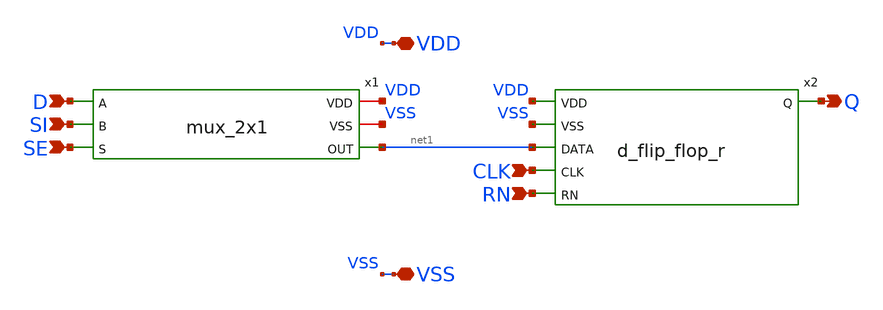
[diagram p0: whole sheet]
** sch_path: designs/cells/sdffrnq/sch/sdffrnq.sch
**.subckt sdffrnq D SI SE VDD VSS Q RN CLK
*.ipin D
*.ipin SI
*.ipin SE
*.iopin VDD
*.iopin VSS
*.opin Q
*.ipin RN
*.ipin CLK
x1 D SI VDD VSS SE net1 mux_2x1
x2 VDD VSS Q net1 CLK RN d_flip_flop_r
**.ends

* expanding   symbol:  cells/sdffrq/sch/mux_2x1.sym # of pins=6
** sym_path: designs/cells/sdffrq/sch/mux_2x1.sym
** sch_path: designs/cells/sdffrq/sch/mux_2x1.sch
.subckt mux_2x1 A B VDD VSS S OUT
*.iopin VDD
*.opin OUT
*.ipin A
*.ipin B
*.ipin S
*.iopin VSS
x1 VDD S A TG_OUT S_INV VSS mux_tg
x2 VDD S_INV B TG_OUT S VSS mux_tg
x3 VDD S S_INV VSS inv
x4 VDD TG_OUT net1 VSS inv
x5 VDD net1 OUT VSS inv
.ends


* expanding   symbol:  cells/sdffrq/sch/d_flip_flop_r.sym # of pins=6
** sym_path: designs/cells/gf180mcu_voidwalkers_sc_sdffrnq_4/sch/d_flip_flop_r.sym
** sch_path: designs/cells/gf180mcu_voidwalkers_sc_sdffrnq_4/sch/d_flip_flop_r.sch
.subckt d_flip_flop_r VDD VSS Q DATA CLK RN
*.ipin DATA
*.ipin VDD
*.ipin VSS
*.opin Q
*.ipin CLK
*.ipin RN
XM1 net1 DATA VDD VDD pfet_03v3 L=0.3u W=1.7u nf=1 ad='int((nf+1)/2) * W/nf * 0.18u' as='int((nf+2)/2) * W/nf * 0.18u'
+ pd='2*int((nf+1)/2) * (W/nf + 0.18u)' ps='2*int((nf+2)/2) * (W/nf + 0.18u)' nrd='0.18u / W' nrs='0.18u / W'
+ sa=0 sb=0 sd=0 m=1
XM2 PROBE[0] CLK_INV net2 VSS nfet_03v3 L=0.3u W=0.85u nf=1 ad='int((nf+1)/2) * W/nf * 0.18u' as='int((nf+2)/2) * W/nf * 0.18u'
+ pd='2*int((nf+1)/2) * (W/nf + 0.18u)' ps='2*int((nf+2)/2) * (W/nf + 0.18u)' nrd='0.18u / W' nrs='0.18u / W'
+ sa=0 sb=0 sd=0 m=1
XM3 PROBE[0] CLK net1 VDD pfet_03v3 L=0.3u W=1.7u nf=1 ad='int((nf+1)/2) * W/nf * 0.18u' as='int((nf+2)/2) * W/nf * 0.18u'
+ pd='2*int((nf+1)/2) * (W/nf + 0.18u)' ps='2*int((nf+2)/2) * (W/nf + 0.18u)' nrd='0.18u / W' nrs='0.18u / W'
+ sa=0 sb=0 sd=0 m=1
XM4 net2 DATA VSS VSS nfet_03v3 L=0.3u W=0.85u nf=1 ad='int((nf+1)/2) * W/nf * 0.18u' as='int((nf+2)/2) * W/nf * 0.18u'
+ pd='2*int((nf+1)/2) * (W/nf + 0.18u)' ps='2*int((nf+2)/2) * (W/nf + 0.18u)' nrd='0.18u / W' nrs='0.18u / W'
+ sa=0 sb=0 sd=0 m=1
XM5 CLK_INV_2 CLK VDD VDD pfet_03v3 L=0.3u W=1.7u nf=1 ad='int((nf+1)/2) * W/nf * 0.18u' as='int((nf+2)/2) * W/nf * 0.18u'
+ pd='2*int((nf+1)/2) * (W/nf + 0.18u)' ps='2*int((nf+2)/2) * (W/nf + 0.18u)' nrd='0.18u / W' nrs='0.18u / W'
+ sa=0 sb=0 sd=0 m=1
XM8 CLK_INV_2 CLK VSS VSS nfet_03v3 L=0.3u W=0.85u nf=1 ad='int((nf+1)/2) * W/nf * 0.18u' as='int((nf+2)/2) * W/nf * 0.18u'
+ pd='2*int((nf+1)/2) * (W/nf + 0.18u)' ps='2*int((nf+2)/2) * (W/nf + 0.18u)' nrd='0.18u / W' nrs='0.18u / W'
+ sa=0 sb=0 sd=0 m=1
XM13 net3 PROBE[1] VDD VDD pfet_03v3 L=0.3u W=1.7u nf=1 ad='int((nf+1)/2) * W/nf * 0.18u' as='int((nf+2)/2) * W/nf * 0.18u'
+ pd='2*int((nf+1)/2) * (W/nf + 0.18u)' ps='2*int((nf+2)/2) * (W/nf + 0.18u)' nrd='0.18u / W' nrs='0.18u / W'
+ sa=0 sb=0 sd=0 m=1
XM14 PROBE[0] CLK net4 VSS nfet_03v3 L=0.3u W=0.85u nf=1 ad='int((nf+1)/2) * W/nf * 0.18u' as='int((nf+2)/2) * W/nf * 0.18u'
+ pd='2*int((nf+1)/2) * (W/nf + 0.18u)' ps='2*int((nf+2)/2) * (W/nf + 0.18u)' nrd='0.18u / W' nrs='0.18u / W'
+ sa=0 sb=0 sd=0 m=1
XM15 PROBE[0] CLK_INV net3 VDD pfet_03v3 L=0.3u W=1.7u nf=1 ad='int((nf+1)/2) * W/nf * 0.18u' as='int((nf+2)/2) * W/nf * 0.18u'
+ pd='2*int((nf+1)/2) * (W/nf + 0.18u)' ps='2*int((nf+2)/2) * (W/nf + 0.18u)' nrd='0.18u / W' nrs='0.18u / W'
+ sa=0 sb=0 sd=0 m=1
XM16 net4 PROBE[1] VSS VSS nfet_03v3 L=0.3u W=0.85u nf=1 ad='int((nf+1)/2) * W/nf * 0.18u' as='int((nf+2)/2) * W/nf * 0.18u'
+ pd='2*int((nf+1)/2) * (W/nf + 0.18u)' ps='2*int((nf+2)/2) * (W/nf + 0.18u)' nrd='0.18u / W' nrs='0.18u / W'
+ sa=0 sb=0 sd=0 m=1
XM9 net5 PROBE[1] VDD VDD pfet_03v3 L=0.3u W=1.7u nf=1 ad='int((nf+1)/2) * W/nf * 0.18u' as='int((nf+2)/2) * W/nf * 0.18u'
+ pd='2*int((nf+1)/2) * (W/nf + 0.18u)' ps='2*int((nf+2)/2) * (W/nf + 0.18u)' nrd='0.18u / W' nrs='0.18u / W'
+ sa=0 sb=0 sd=0 m=1
XM10 PROBE[2] CLK net6 VSS nfet_03v3 L=0.3u W=0.85u nf=1 ad='int((nf+1)/2) * W/nf * 0.18u' as='int((nf+2)/2) * W/nf * 0.18u'
+ pd='2*int((nf+1)/2) * (W/nf + 0.18u)' ps='2*int((nf+2)/2) * (W/nf + 0.18u)' nrd='0.18u / W' nrs='0.18u / W'
+ sa=0 sb=0 sd=0 m=1
XM11 PROBE[2] CLK_INV_2 net5 VDD pfet_03v3 L=0.3u W=1.7u nf=1 ad='int((nf+1)/2) * W/nf * 0.18u' as='int((nf+2)/2) * W/nf * 0.18u'
+ pd='2*int((nf+1)/2) * (W/nf + 0.18u)' ps='2*int((nf+2)/2) * (W/nf + 0.18u)' nrd='0.18u / W' nrs='0.18u / W'
+ sa=0 sb=0 sd=0 m=1
XM12 net6 PROBE[1] VSS VSS nfet_03v3 L=0.3u W=0.85u nf=1 ad='int((nf+1)/2) * W/nf * 0.18u' as='int((nf+2)/2) * W/nf * 0.18u'
+ pd='2*int((nf+1)/2) * (W/nf + 0.18u)' ps='2*int((nf+2)/2) * (W/nf + 0.18u)' nrd='0.18u / W' nrs='0.18u / W'
+ sa=0 sb=0 sd=0 m=1
XM19 net7 PROBE[3] VDD VDD pfet_03v3 L=0.3u W=1.7u nf=1 ad='int((nf+1)/2) * W/nf * 0.18u' as='int((nf+2)/2) * W/nf * 0.18u'
+ pd='2*int((nf+1)/2) * (W/nf + 0.18u)' ps='2*int((nf+2)/2) * (W/nf + 0.18u)' nrd='0.18u / W' nrs='0.18u / W'
+ sa=0 sb=0 sd=0 m=1
XM20 PROBE[2] CLK_INV_2 net8 VSS nfet_03v3 L=0.3u W=0.85u nf=1 ad='int((nf+1)/2) * W/nf * 0.18u' as='int((nf+2)/2) * W/nf * 0.18u'
+ pd='2*int((nf+1)/2) * (W/nf + 0.18u)' ps='2*int((nf+2)/2) * (W/nf + 0.18u)' nrd='0.18u / W' nrs='0.18u / W'
+ sa=0 sb=0 sd=0 m=1
XM21 PROBE[2] CLK net7 VDD pfet_03v3 L=0.3u W=1.7u nf=1 ad='int((nf+1)/2) * W/nf * 0.18u' as='int((nf+2)/2) * W/nf * 0.18u'
+ pd='2*int((nf+1)/2) * (W/nf + 0.18u)' ps='2*int((nf+2)/2) * (W/nf + 0.18u)' nrd='0.18u / W' nrs='0.18u / W'
+ sa=0 sb=0 sd=0 m=1
XM22 net8 PROBE[3] VSS VSS nfet_03v3 L=0.3u W=0.85u nf=1 ad='int((nf+1)/2) * W/nf * 0.18u' as='int((nf+2)/2) * W/nf * 0.18u'
+ pd='2*int((nf+1)/2) * (W/nf + 0.18u)' ps='2*int((nf+2)/2) * (W/nf + 0.18u)' nrd='0.18u / W' nrs='0.18u / W'
+ sa=0 sb=0 sd=0 m=1
XM23 QN PROBE[3] VDD VDD pfet_03v3 L=0.3u W=1.7u nf=1 ad='int((nf+1)/2) * W/nf * 0.18u' as='int((nf+2)/2) * W/nf * 0.18u'
+ pd='2*int((nf+1)/2) * (W/nf + 0.18u)' ps='2*int((nf+2)/2) * (W/nf + 0.18u)' nrd='0.18u / W' nrs='0.18u / W'
+ sa=0 sb=0 sd=0 m=1
XM24 QN PROBE[3] VSS VSS nfet_03v3 L=0.3u W=0.85u nf=1 ad='int((nf+1)/2) * W/nf * 0.18u' as='int((nf+2)/2) * W/nf * 0.18u'
+ pd='2*int((nf+1)/2) * (W/nf + 0.18u)' ps='2*int((nf+2)/2) * (W/nf + 0.18u)' nrd='0.18u / W' nrs='0.18u / W'
+ sa=0 sb=0 sd=0 m=1
XM25 Q QN VDD VDD pfet_03v3 L=0.3u W=1.7u nf=1 ad='int((nf+1)/2) * W/nf * 0.18u' as='int((nf+2)/2) * W/nf * 0.18u'
+ pd='2*int((nf+1)/2) * (W/nf + 0.18u)' ps='2*int((nf+2)/2) * (W/nf + 0.18u)' nrd='0.18u / W' nrs='0.18u / W'
+ sa=0 sb=0 sd=0 m=1
XM26 Q QN VSS VSS nfet_03v3 L=0.3u W=0.85u nf=1 ad='int((nf+1)/2) * W/nf * 0.18u' as='int((nf+2)/2) * W/nf * 0.18u'
+ pd='2*int((nf+1)/2) * (W/nf + 0.18u)' ps='2*int((nf+2)/2) * (W/nf + 0.18u)' nrd='0.18u / W' nrs='0.18u / W'
+ sa=0 sb=0 sd=0 m=1
XM6 net9 PROBE[0] VDD VDD pfet_03v3 L=0.3u W=1.7u nf=1 ad='int((nf+1)/2) * W/nf * 0.18u' as='int((nf+2)/2) * W/nf * 0.18u'
+ pd='2*int((nf+1)/2) * (W/nf + 0.18u)' ps='2*int((nf+2)/2) * (W/nf + 0.18u)' nrd='0.18u / W' nrs='0.18u / W'
+ sa=0 sb=0 sd=0 m=1
XM27 PROBE[1] R net9 VDD pfet_03v3 L=0.3u W=1.7u nf=1 ad='int((nf+1)/2) * W/nf * 0.18u' as='int((nf+2)/2) * W/nf * 0.18u'
+ pd='2*int((nf+1)/2) * (W/nf + 0.18u)' ps='2*int((nf+2)/2) * (W/nf + 0.18u)' nrd='0.18u / W' nrs='0.18u / W'
+ sa=0 sb=0 sd=0 m=1
XM28 PROBE[1] PROBE[0] VSS VSS nfet_03v3 L=0.3u W=0.85u nf=1 ad='int((nf+1)/2) * W/nf * 0.18u' as='int((nf+2)/2) * W/nf * 0.18u'
+ pd='2*int((nf+1)/2) * (W/nf + 0.18u)' ps='2*int((nf+2)/2) * (W/nf + 0.18u)' nrd='0.18u / W' nrs='0.18u / W'
+ sa=0 sb=0 sd=0 m=1
XM17 net10 PROBE[2] VDD VDD pfet_03v3 L=0.3u W=1.7u nf=1 ad='int((nf+1)/2) * W/nf * 0.18u' as='int((nf+2)/2) * W/nf * 0.18u'
+ pd='2*int((nf+1)/2) * (W/nf + 0.18u)' ps='2*int((nf+2)/2) * (W/nf + 0.18u)' nrd='0.18u / W' nrs='0.18u / W'
+ sa=0 sb=0 sd=0 m=1
XM29 PROBE[3] R net10 VDD pfet_03v3 L=0.3u W=1.7u nf=1 ad='int((nf+1)/2) * W/nf * 0.18u' as='int((nf+2)/2) * W/nf * 0.18u'
+ pd='2*int((nf+1)/2) * (W/nf + 0.18u)' ps='2*int((nf+2)/2) * (W/nf + 0.18u)' nrd='0.18u / W' nrs='0.18u / W'
+ sa=0 sb=0 sd=0 m=1
XM30 PROBE[3] PROBE[2] VSS VSS nfet_03v3 L=0.3u W=0.85u nf=1 ad='int((nf+1)/2) * W/nf * 0.18u' as='int((nf+2)/2) * W/nf * 0.18u'
+ pd='2*int((nf+1)/2) * (W/nf + 0.18u)' ps='2*int((nf+2)/2) * (W/nf + 0.18u)' nrd='0.18u / W' nrs='0.18u / W'
+ sa=0 sb=0 sd=0 m=1
XM7 PROBE[1] R VSS VSS nfet_03v3 L=0.3u W=0.85u nf=1 ad='int((nf+1)/2) * W/nf * 0.18u' as='int((nf+2)/2) * W/nf * 0.18u'
+ pd='2*int((nf+1)/2) * (W/nf + 0.18u)' ps='2*int((nf+2)/2) * (W/nf + 0.18u)' nrd='0.18u / W' nrs='0.18u / W'
+ sa=0 sb=0 sd=0 m=1
XM18 PROBE[3] R VSS VSS nfet_03v3 L=0.3u W=0.85u nf=1 ad='int((nf+1)/2) * W/nf * 0.18u' as='int((nf+2)/2) * W/nf * 0.18u'
+ pd='2*int((nf+1)/2) * (W/nf + 0.18u)' ps='2*int((nf+2)/2) * (W/nf + 0.18u)' nrd='0.18u / W' nrs='0.18u / W'
+ sa=0 sb=0 sd=0 m=1
XM31 R RN VDD VDD pfet_03v3 L=0.3u W=1.7u nf=1 ad='int((nf+1)/2) * W/nf * 0.18u' as='int((nf+2)/2) * W/nf * 0.18u'
+ pd='2*int((nf+1)/2) * (W/nf + 0.18u)' ps='2*int((nf+2)/2) * (W/nf + 0.18u)' nrd='0.18u / W' nrs='0.18u / W'
+ sa=0 sb=0 sd=0 m=1
XM32 R RN VSS VSS nfet_03v3 L=0.3u W=0.85u nf=1 ad='int((nf+1)/2) * W/nf * 0.18u' as='int((nf+2)/2) * W/nf * 0.18u'
+ pd='2*int((nf+1)/2) * (W/nf + 0.18u)' ps='2*int((nf+2)/2) * (W/nf + 0.18u)' nrd='0.18u / W' nrs='0.18u / W'
+ sa=0 sb=0 sd=0 m=1
XM33 CLK_INV CLK VDD VDD pfet_03v3 L=0.3u W=1.7u nf=1 ad='int((nf+1)/2) * W/nf * 0.18u' as='int((nf+2)/2) * W/nf * 0.18u'
+ pd='2*int((nf+1)/2) * (W/nf + 0.18u)' ps='2*int((nf+2)/2) * (W/nf + 0.18u)' nrd='0.18u / W' nrs='0.18u / W'
+ sa=0 sb=0 sd=0 m=1
XM34 CLK_INV CLK VSS VSS nfet_03v3 L=0.3u W=0.85u nf=1 ad='int((nf+1)/2) * W/nf * 0.18u' as='int((nf+2)/2) * W/nf * 0.18u'
+ pd='2*int((nf+1)/2) * (W/nf + 0.18u)' ps='2*int((nf+2)/2) * (W/nf + 0.18u)' nrd='0.18u / W' nrs='0.18u / W'
+ sa=0 sb=0 sd=0 m=1
.ends


* expanding   symbol:  mux_tg.sym # of pins=6
** sym_path: designs/cells/sdffrq/sch/mux_tg.sym
** sch_path: designs/cells/sdffrq/sch/mux_tg.sch
.subckt mux_tg VDD P_GATE IN OUT N_GATE VSS
*.iopin VDD
*.iopin VSS
*.opin OUT
*.ipin IN
*.ipin P_GATE
*.ipin N_GATE
XM1 IN N_GATE OUT VSS nfet_03v3 L=0.3u W=0.85u nf=1 ad='int((nf+1)/2) * W/nf * 0.18u' as='int((nf+2)/2) * W/nf * 0.18u'
+ pd='2*int((nf+1)/2) * (W/nf + 0.18u)' ps='2*int((nf+2)/2) * (W/nf + 0.18u)' nrd='0.18u / W' nrs='0.18u / W'
+ sa=0 sb=0 sd=0 m=1
XM2 IN P_GATE OUT VDD pfet_03v3 L=0.3u W=1.7u nf=1 ad='int((nf+1)/2) * W/nf * 0.18u' as='int((nf+2)/2) * W/nf * 0.18u'
+ pd='2*int((nf+1)/2) * (W/nf + 0.18u)' ps='2*int((nf+2)/2) * (W/nf + 0.18u)' nrd='0.18u / W' nrs='0.18u / W'
+ sa=0 sb=0 sd=0 m=1
.ends


* expanding   symbol:  inv.sym # of pins=4
** sym_path: designs/libs/mux2x1/inv.sym
** sch_path: designs/libs/mux2x1/inv.sch
.subckt inv VDD IN OUT VSS
*.ipin IN
*.opin OUT
*.iopin VDD
*.iopin VSS
XM2 OUT IN VDD VDD pfet_03v3 L=0.3u W=1.7u nf=1 ad='int((nf+1)/2) * W/nf * 0.18u' as='int((nf+2)/2) * W/nf * 0.18u'
+ pd='2*int((nf+1)/2) * (W/nf + 0.18u)' ps='2*int((nf+2)/2) * (W/nf + 0.18u)' nrd='0.18u / W' nrs='0.18u / W'
+ sa=0 sb=0 sd=0 m=1
XM1 OUT IN VSS VSS nfet_03v3 L=0.3u W=0.85u nf=1 ad='int((nf+1)/2) * W/nf * 0.18u' as='int((nf+2)/2) * W/nf * 0.18u'
+ pd='2*int((nf+1)/2) * (W/nf + 0.18u)' ps='2*int((nf+2)/2) * (W/nf + 0.18u)' nrd='0.18u / W' nrs='0.18u / W'
+ sa=0 sb=0 sd=0 m=1
.ends

.end
